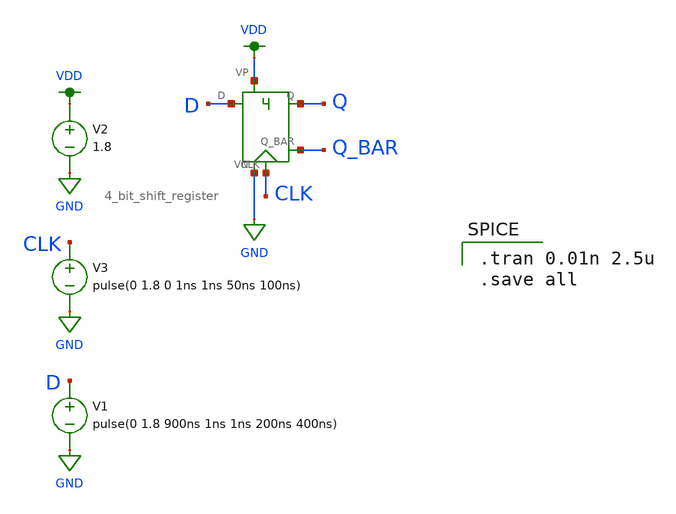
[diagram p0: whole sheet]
** sch_path: mp2/schematics/4_bit_shift_register_tran.sch
**.subckt 4_bit_shift_register_tran
V1 D GND pulse(0 1.8 900ns 1ns 1ns 200ns 400ns)
V2 VDD GND 1.8
V3 CLK GND pulse(0 1.8 0 1ns 1ns 50ns 100ns)
X1 D Q_BAR VDD Q CLK GND 4_bit_shift_register
**** begin user architecture code

.option wnflag=1
.lib ~/skywater/skywater-pdk/libraries/sky130_fd_pr_ngspice/latest/models/sky130.lib.spice tt


.tran 0.01n 2.5u
.save all

**** end user architecture code
**.ends
.GLOBAL GND
.GLOBAL VDD
.end
